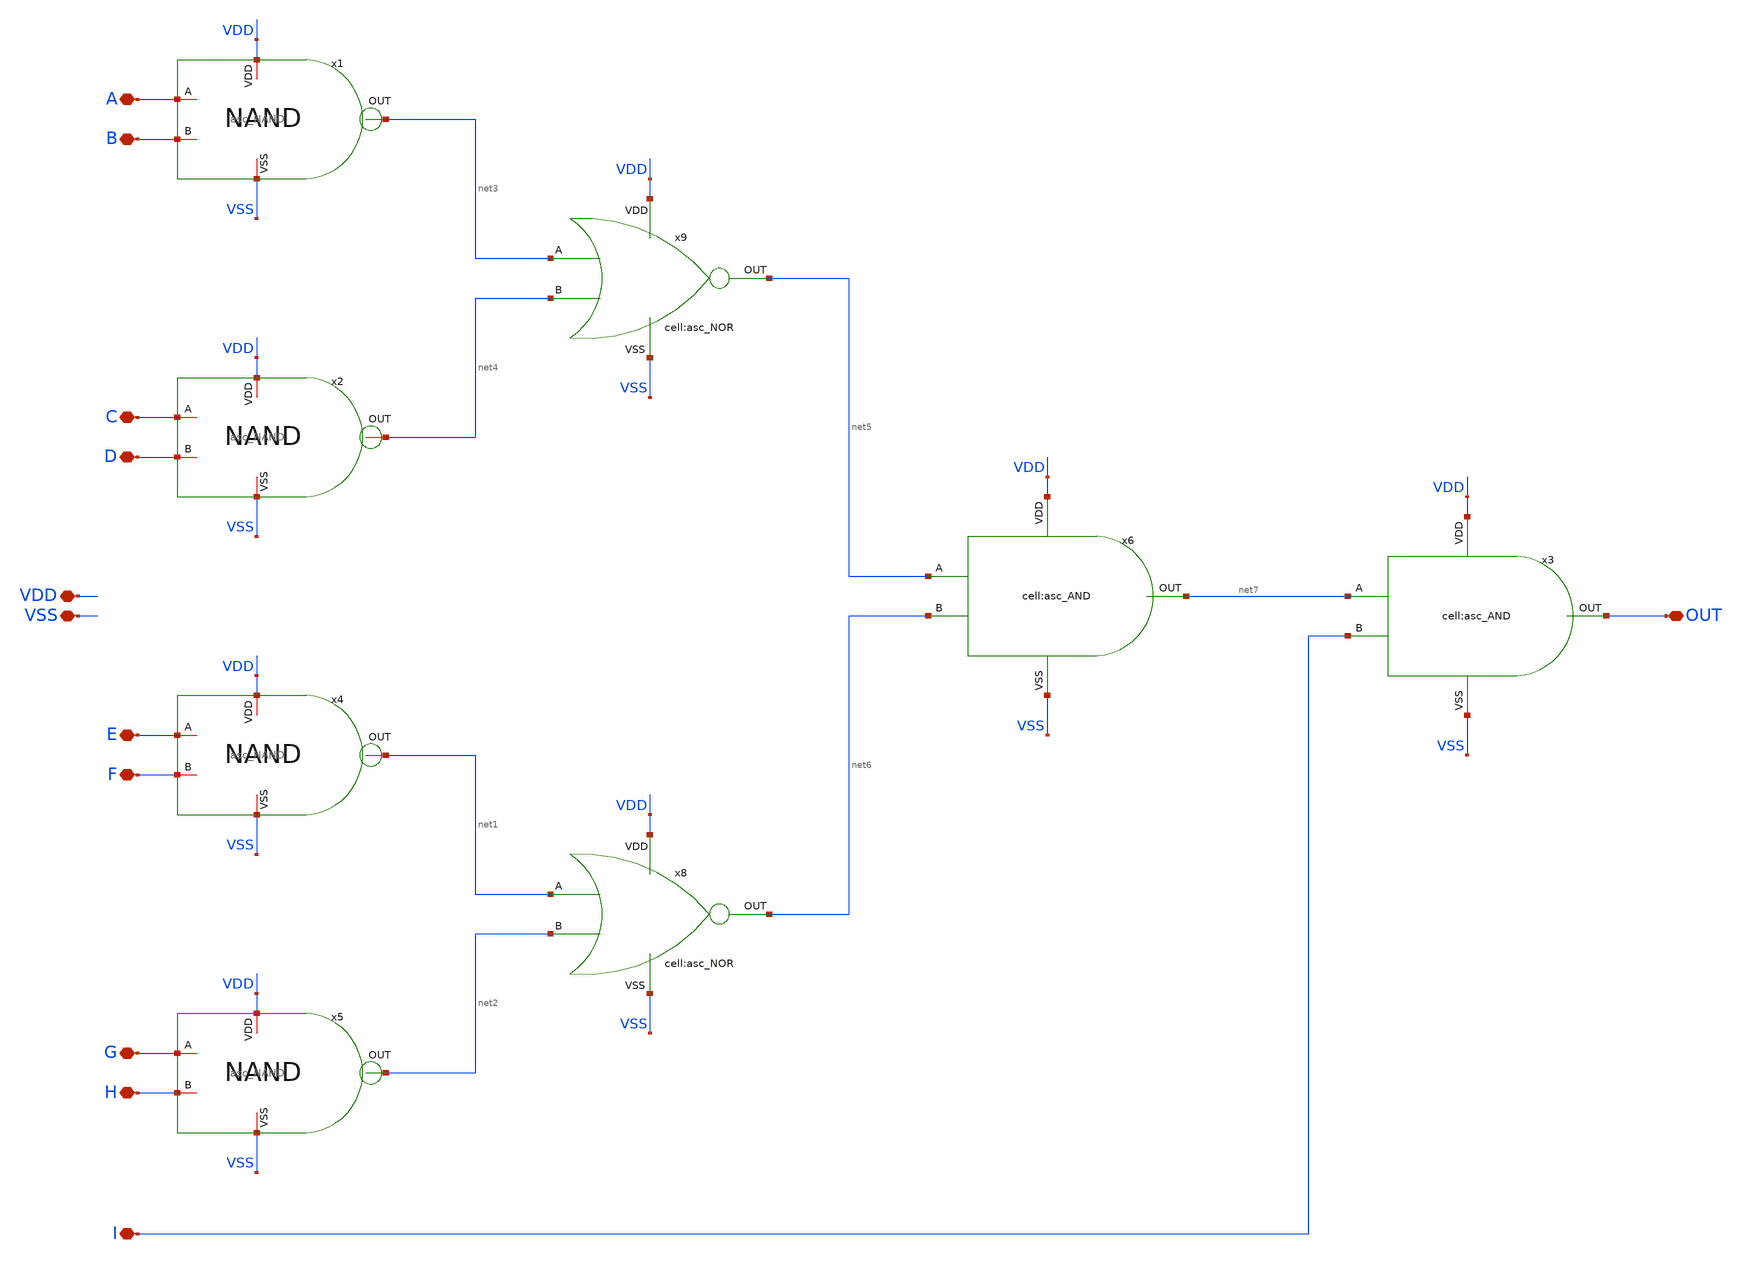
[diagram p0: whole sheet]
** sch_path: designs/libs/core_analog/asc_AND_9_20250809/asc_AND_9_20250809.sch
**.subckt asc_AND_9_20250809 VDD VSS B A D C F E H G I OUT
*.iopin VDD
*.iopin VSS
*.iopin B
*.iopin A
*.iopin D
*.iopin C
*.iopin F
*.iopin E
*.iopin H
*.iopin G
*.iopin I
*.iopin OUT
x3 VDD OUT net7 I VSS asc_AND
x1 VDD net3 A B VSS asc_NAND
x2 VDD net4 C D VSS asc_NAND
x4 VDD net1 E F VSS asc_NAND
x5 VDD net2 G H VSS asc_NAND
x8 VDD VSS net6 net1 net2 asc_NOR
x9 VDD VSS net5 net3 net4 asc_NOR
x6 VDD net7 net5 net6 VSS asc_AND
**.ends
.end
